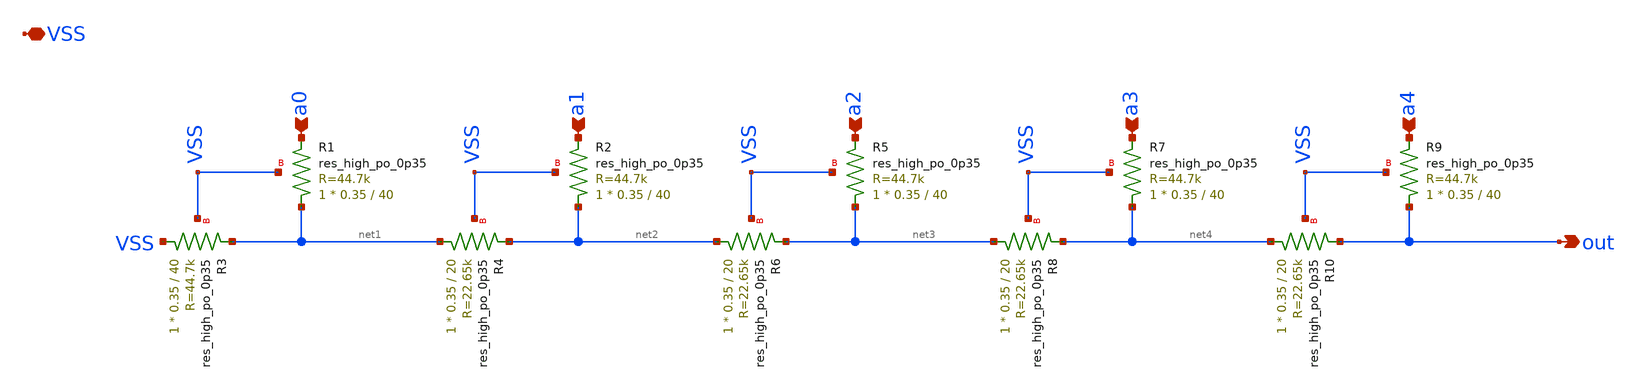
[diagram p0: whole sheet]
** sch_path: xschem/dac_5b.sch
**.subckt dac_5b VSS a0 a1 a2 a3 a4 out
*.iopin VSS
*.ipin a0
*.ipin a1
*.ipin a2
*.ipin a3
*.ipin a4
*.opin out
XR1 net1 a0 VSS sky130_fd_pr__res_high_po_0p35 L=40 mult=1 m=1
XR3 VSS net1 VSS sky130_fd_pr__res_high_po_0p35 L=40 mult=1 m=1
XR2 net2 a1 VSS sky130_fd_pr__res_high_po_0p35 L=40 mult=1 m=1
XR4 net1 net2 VSS sky130_fd_pr__res_high_po_0p35 L=20 mult=1 m=1
XR5 net3 a2 VSS sky130_fd_pr__res_high_po_0p35 L=40 mult=1 m=1
XR6 net2 net3 VSS sky130_fd_pr__res_high_po_0p35 L=20 mult=1 m=1
XR7 net4 a3 VSS sky130_fd_pr__res_high_po_0p35 L=40 mult=1 m=1
XR8 net3 net4 VSS sky130_fd_pr__res_high_po_0p35 L=20 mult=1 m=1
XR9 out a4 VSS sky130_fd_pr__res_high_po_0p35 L=40 mult=1 m=1
XR10 net4 out VSS sky130_fd_pr__res_high_po_0p35 L=20 mult=1 m=1
**.ends
.end
